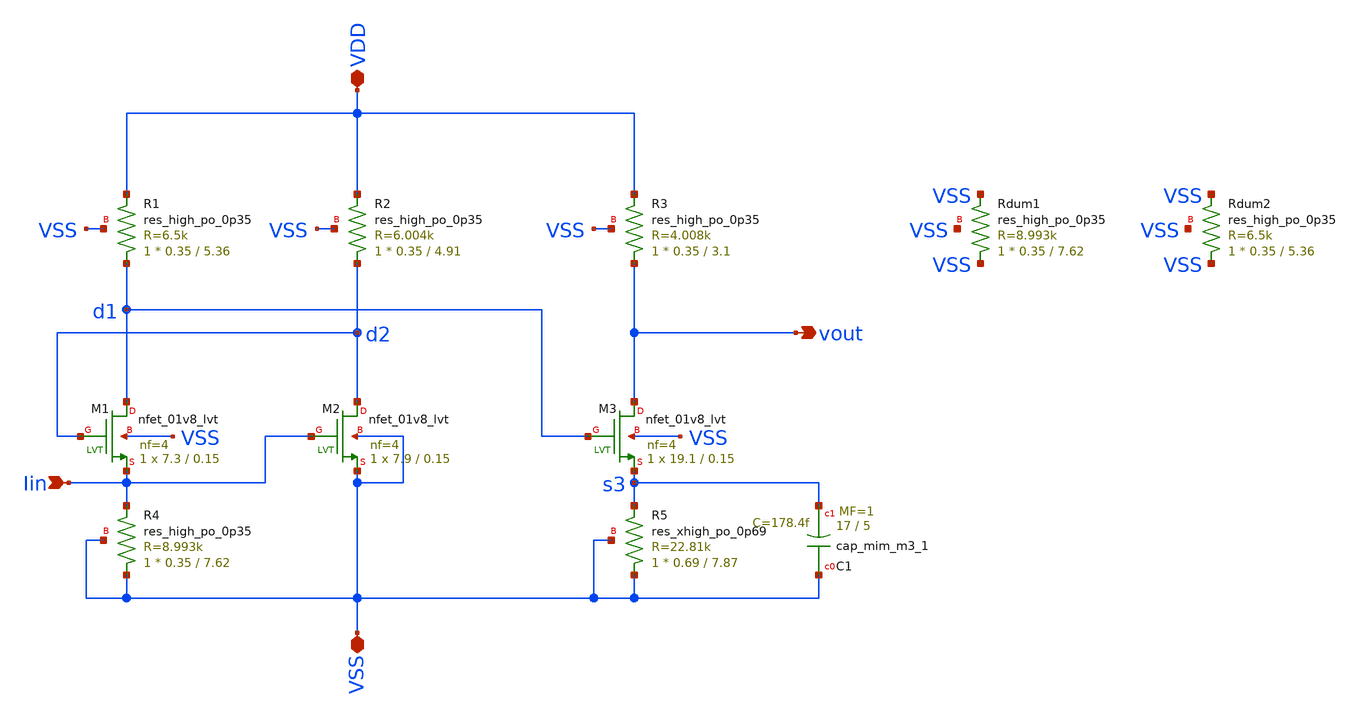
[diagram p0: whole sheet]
** sch_path: ip/tia.sch
**.subckt tia Iin vout VDD VSS
*.ipin Iin
*.opin vout
*.iopin VDD
*.iopin VSS
XM1 d1 d2 Iin VSS sky130_fd_pr__nfet_01v8_lvt L=0.15 W=7.3 nf=4 ad=0 as=0 pd=0 ps=0 nrd=0 nrs=0 sa=0
+ sb=0 sd=0 mult=1 m=1
XM2 d2 Iin VSS VSS sky130_fd_pr__nfet_01v8_lvt L=0.15 W=7.9 nf=4 ad=0 as=0 pd=0 ps=0 nrd=0 nrs=0
+ sa=0 sb=0 sd=0 mult=1 m=1
XM3 vout d1 s3 VSS sky130_fd_pr__nfet_01v8_lvt L=0.15 W=19.1 nf=4 ad=0 as=0 pd=0 ps=0 nrd=0 nrs=0
+ sa=0 sb=0 sd=0 mult=1 m=1
XR1 d1 VDD VSS sky130_fd_pr__res_high_po_0p35 L=5.36 mult=1 m=1
XR2 d2 VDD VSS sky130_fd_pr__res_high_po_0p35 L=4.91 mult=1 m=1
XR3 vout VDD VSS sky130_fd_pr__res_high_po_0p35 L=3.1 mult=1 m=1
XR4 VSS Iin VSS sky130_fd_pr__res_high_po_0p35 L=7.62 mult=1 m=1
XR5 VSS s3 VSS sky130_fd_pr__res_xhigh_po_0p69 L=7.87 mult=1 m=1
XC1 VSS s3 sky130_fd_pr__cap_mim_m3_1 W=17 L=5 MF=1 m=1
XRdum1 VSS VSS VSS sky130_fd_pr__res_high_po_0p35 L=7.62 mult=1 m=1
XRdum2 VSS VSS VSS sky130_fd_pr__res_high_po_0p35 L=5.36 mult=1 m=1
**.ends
.end
